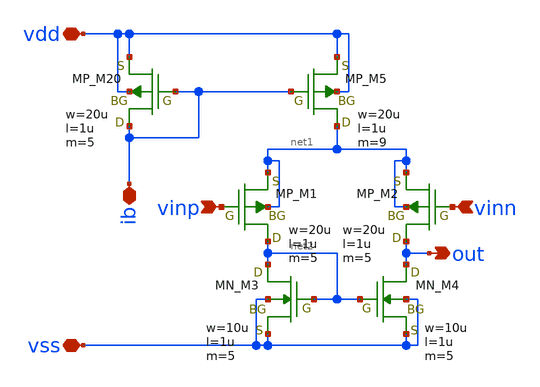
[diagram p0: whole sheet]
** sch_path: member_project/Tiny555/yamada3/xschem/comparator.sch
**.subckt comparator vdd ib vinp vinn vss out
*.iopin vdd
*.iopin ib
*.ipin vinp
*.ipin vinn
*.iopin vss
*.opin out
XM5 net1 ib vdd vdd PMOS w=20u l=1u as=0 ad=0 ps=0 pd=0 nrd=0 nrs=0 m=9
XM20 ib ib vdd vdd PMOS w=20u l=1u as=0 ad=0 ps=0 pd=0 nrd=0 nrs=0 m=5
XM1 net2 vinp net1 net1 PMOS w=20u l=1u as=0 ad=0 ps=0 pd=0 nrd=0 nrs=0 m=5
XM2 out vinn net1 net1 PMOS w=20u l=1u as=0 ad=0 ps=0 pd=0 nrd=0 nrs=0 m=5
XM3 net2 net2 vss vss NMOS w=10u l=1u as=0 ad=0 ps=0 pd=0 nrd=0 nrs=0 m=5
XM4 out net2 vss vss NMOS w=10u l=1u as=0 ad=0 ps=0 pd=0 nrd=0 nrs=0 m=5
**.ends
.end
